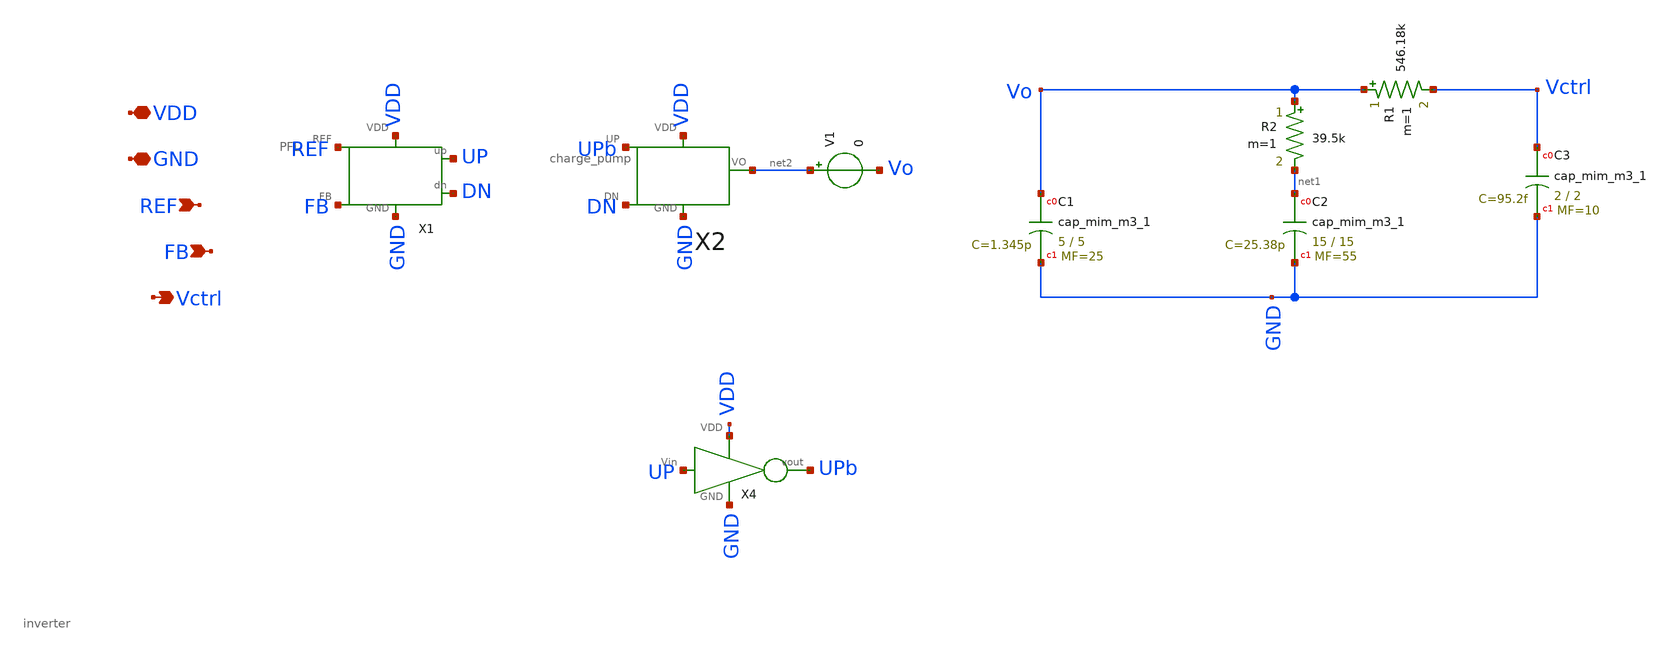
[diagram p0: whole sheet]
** sch_path: pll/pfd_cp_lf_lib/PFD_CP_LPF/Xschem/PFD_CP_LPF.sch
**.subckt PFD_CP_LPF VDD GND REF FB Vctrl
*.iopin VDD
*.iopin GND
*.ipin REF
*.ipin FB
*.opin Vctrl
XC1 Vo GND sky130_fd_pr__cap_mim_m3_1 W=5 L=5 MF=25 m=25
XC2 net1 GND sky130_fd_pr__cap_mim_m3_1 W=15 L=15 MF=55 m=55
XC3 Vctrl GND sky130_fd_pr__cap_mim_m3_1 W=2 L=2 MF=10 m=10
X1 REF UP FB VDD GND DN PFD
X2 DN UPb net2 GND VDD charge_pump
X4 UP UPb VDD GND inverter
R2 Vo net1 39.5k m=1
R1 Vo Vctrl 546.18k m=1
V1 net2 Vo 0
**.ends
.end
